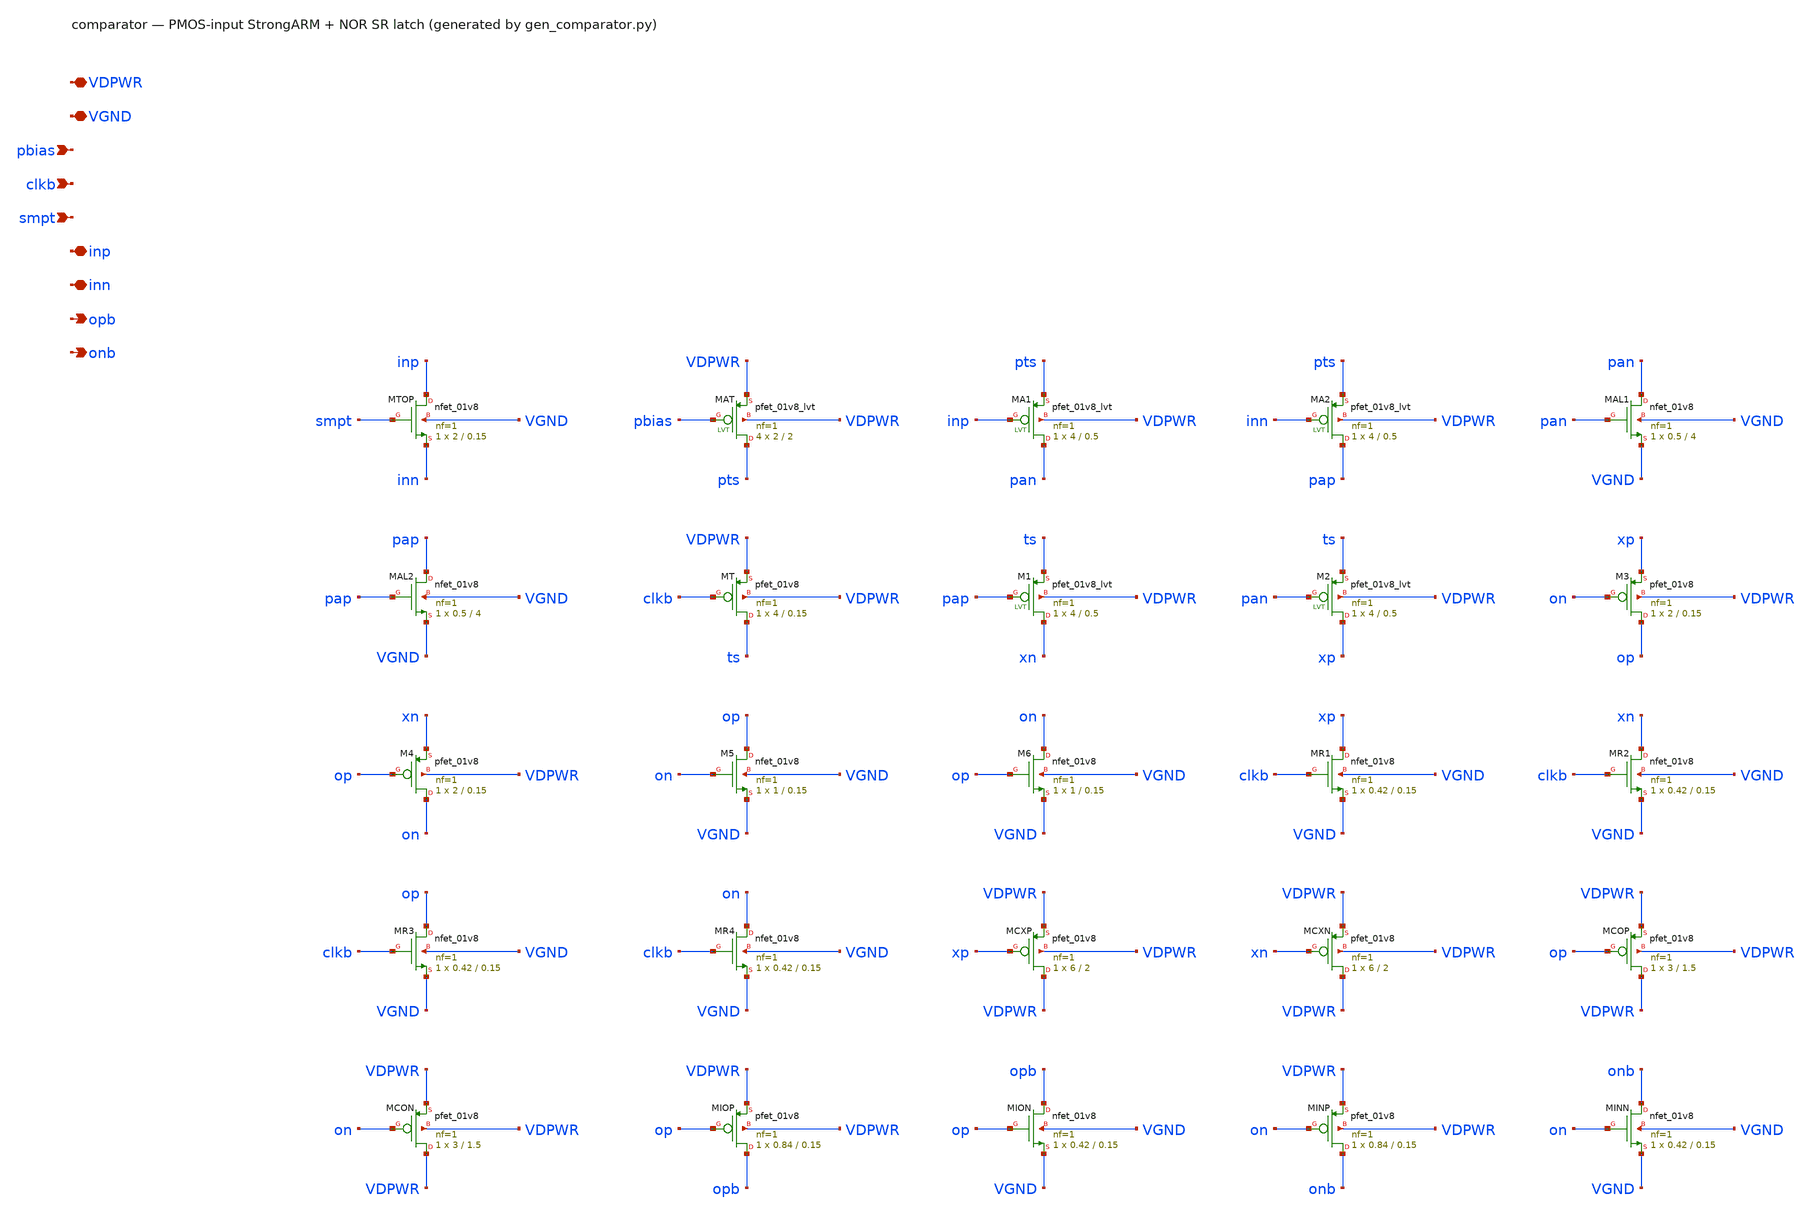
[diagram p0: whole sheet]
** sch_path: xschem/comparator.sch
**.subckt comparator VDPWR VGND pbias clkb smpt inp inn opb onb
*.iopin VDPWR
*.iopin VGND
*.ipin pbias
*.ipin clkb
*.ipin smpt
*.iopin inp
*.iopin inn
*.opin opb
*.opin onb
XMTOP inp smpt inn VGND sky130_fd_pr__nfet_01v8 L=0.15 W=2 nf=1 ad='int((1 + 1)/2) * 2 / 1 * 0.29' as='int((1 + 2)/2) * 2 / 1 * 0.29'
+ pd='2*int((1 + 1)/2) * (2 / 1 + 0.29)' ps='2*int((1 + 2)/2) * (2 / 1 + 0.29)' nrd='0.29 / 2 ' nrs='0.29 / 2 '
+ sa=0 sb=0 sd=0 mult=1 m=1
XMAT pts pbias VDPWR VDPWR sky130_fd_pr__pfet_01v8_lvt L=2 W=2 nf=1 ad='int((1 + 1)/2) * 2 / 1 * 0.29'
+ as='int((1 + 2)/2) * 2 / 1 * 0.29' pd='2*int((1 + 1)/2) * (2 / 1 + 0.29)' ps='2*int((1 + 2)/2) * (2 / 1 + 0.29)'
+ nrd='0.29 / 2 ' nrs='0.29 / 2 ' sa=0 sb=0 sd=0 mult=4 m=4
XMA1 pan inp pts VDPWR sky130_fd_pr__pfet_01v8_lvt L=0.5 W=4 nf=1 ad='int((1 + 1)/2) * 4 / 1 * 0.29'
+ as='int((1 + 2)/2) * 4 / 1 * 0.29' pd='2*int((1 + 1)/2) * (4 / 1 + 0.29)' ps='2*int((1 + 2)/2) * (4 / 1 + 0.29)'
+ nrd='0.29 / 4 ' nrs='0.29 / 4 ' sa=0 sb=0 sd=0 mult=1 m=1
XMA2 pap inn pts VDPWR sky130_fd_pr__pfet_01v8_lvt L=0.5 W=4 nf=1 ad='int((1 + 1)/2) * 4 / 1 * 0.29'
+ as='int((1 + 2)/2) * 4 / 1 * 0.29' pd='2*int((1 + 1)/2) * (4 / 1 + 0.29)' ps='2*int((1 + 2)/2) * (4 / 1 + 0.29)'
+ nrd='0.29 / 4 ' nrs='0.29 / 4 ' sa=0 sb=0 sd=0 mult=1 m=1
XMAL1 pan pan VGND VGND sky130_fd_pr__nfet_01v8 L=4 W=0.5 nf=1 ad='int((1 + 1)/2) * 0.5 / 1 * 0.29' as='int((1 + 2)/2) * 0.5 / 1 * 0.29'
+ pd='2*int((1 + 1)/2) * (0.5 / 1 + 0.29)' ps='2*int((1 + 2)/2) * (0.5 / 1 + 0.29)' nrd='0.29 / 0.5 ' nrs='0.29 / 0.5 '
+ sa=0 sb=0 sd=0 mult=1 m=1
XMAL2 pap pap VGND VGND sky130_fd_pr__nfet_01v8 L=4 W=0.5 nf=1 ad='int((1 + 1)/2) * 0.5 / 1 * 0.29' as='int((1 + 2)/2) * 0.5 / 1 * 0.29'
+ pd='2*int((1 + 1)/2) * (0.5 / 1 + 0.29)' ps='2*int((1 + 2)/2) * (0.5 / 1 + 0.29)' nrd='0.29 / 0.5 ' nrs='0.29 / 0.5 '
+ sa=0 sb=0 sd=0 mult=1 m=1
XMT ts clkb VDPWR VDPWR sky130_fd_pr__pfet_01v8 L=0.15 W=4 nf=1 ad='int((nf+1)/2) * W/nf * 0.29' as='int((nf+2)/2) * W/nf * 0.29'
+ pd='2*int((nf+1)/2) * (W/nf + 0.29)' ps='2*int((nf+2)/2) * (W/nf + 0.29)' nrd='0.29 / W' nrs='0.29 / W'
+ sa=0 sb=0 sd=0 mult=1 m=1
XM1 xn pap ts VDPWR sky130_fd_pr__pfet_01v8_lvt L=0.5 W=4 nf=1 ad='int((1 + 1)/2) * 4 / 1 * 0.29' as='int((1 + 2)/2) * 4 / 1 * 0.29'
+ pd='2*int((1 + 1)/2) * (4 / 1 + 0.29)' ps='2*int((1 + 2)/2) * (4 / 1 + 0.29)' nrd='0.29 / 4 ' nrs='0.29 / 4 '
+ sa=0 sb=0 sd=0 mult=1 m=1
XM2 xp pan ts VDPWR sky130_fd_pr__pfet_01v8_lvt L=0.5 W=4 nf=1 ad='int((1 + 1)/2) * 4 / 1 * 0.29' as='int((1 + 2)/2) * 4 / 1 * 0.29'
+ pd='2*int((1 + 1)/2) * (4 / 1 + 0.29)' ps='2*int((1 + 2)/2) * (4 / 1 + 0.29)' nrd='0.29 / 4 ' nrs='0.29 / 4 '
+ sa=0 sb=0 sd=0 mult=1 m=1
XM3 op on xp VDPWR sky130_fd_pr__pfet_01v8 L=0.15 W=2 nf=1 ad='int((nf+1)/2) * W/nf * 0.29' as='int((nf+2)/2) * W/nf * 0.29'
+ pd='2*int((nf+1)/2) * (W/nf + 0.29)' ps='2*int((nf+2)/2) * (W/nf + 0.29)' nrd='0.29 / W' nrs='0.29 / W'
+ sa=0 sb=0 sd=0 mult=1 m=1
XM4 on op xn VDPWR sky130_fd_pr__pfet_01v8 L=0.15 W=2 nf=1 ad='int((nf+1)/2) * W/nf * 0.29' as='int((nf+2)/2) * W/nf * 0.29'
+ pd='2*int((nf+1)/2) * (W/nf + 0.29)' ps='2*int((nf+2)/2) * (W/nf + 0.29)' nrd='0.29 / W' nrs='0.29 / W'
+ sa=0 sb=0 sd=0 mult=1 m=1
XM5 op on VGND VGND sky130_fd_pr__nfet_01v8 L=0.15 W=1 nf=1 ad='int((1 + 1)/2) * 1 / 1 * 0.29' as='int((1 + 2)/2) * 1 / 1 * 0.29'
+ pd='2*int((1 + 1)/2) * (1 / 1 + 0.29)' ps='2*int((1 + 2)/2) * (1 / 1 + 0.29)' nrd='0.29 / 1 ' nrs='0.29 / 1 '
+ sa=0 sb=0 sd=0 mult=1 m=1
XM6 on op VGND VGND sky130_fd_pr__nfet_01v8 L=0.15 W=1 nf=1 ad='int((1 + 1)/2) * 1 / 1 * 0.29' as='int((1 + 2)/2) * 1 / 1 * 0.29'
+ pd='2*int((1 + 1)/2) * (1 / 1 + 0.29)' ps='2*int((1 + 2)/2) * (1 / 1 + 0.29)' nrd='0.29 / 1 ' nrs='0.29 / 1 '
+ sa=0 sb=0 sd=0 mult=1 m=1
XMR1 xp clkb VGND VGND sky130_fd_pr__nfet_01v8 L=0.15 W=0.42 nf=1 ad='int((1 + 1)/2) * 0.42 / 1 * 0.29'
+ as='int((1 + 2)/2) * 0.42 / 1 * 0.29' pd='2*int((1 + 1)/2) * (0.42 / 1 + 0.29)' ps='2*int((1 + 2)/2) * (0.42 / 1 + 0.29)'
+ nrd='0.29 / 0.42 ' nrs='0.29 / 0.42 ' sa=0 sb=0 sd=0 mult=1 m=1
XMR2 xn clkb VGND VGND sky130_fd_pr__nfet_01v8 L=0.15 W=0.42 nf=1 ad='int((1 + 1)/2) * 0.42 / 1 * 0.29'
+ as='int((1 + 2)/2) * 0.42 / 1 * 0.29' pd='2*int((1 + 1)/2) * (0.42 / 1 + 0.29)' ps='2*int((1 + 2)/2) * (0.42 / 1 + 0.29)'
+ nrd='0.29 / 0.42 ' nrs='0.29 / 0.42 ' sa=0 sb=0 sd=0 mult=1 m=1
XMR3 op clkb VGND VGND sky130_fd_pr__nfet_01v8 L=0.15 W=0.42 nf=1 ad='int((1 + 1)/2) * 0.42 / 1 * 0.29'
+ as='int((1 + 2)/2) * 0.42 / 1 * 0.29' pd='2*int((1 + 1)/2) * (0.42 / 1 + 0.29)' ps='2*int((1 + 2)/2) * (0.42 / 1 + 0.29)'
+ nrd='0.29 / 0.42 ' nrs='0.29 / 0.42 ' sa=0 sb=0 sd=0 mult=1 m=1
XMR4 on clkb VGND VGND sky130_fd_pr__nfet_01v8 L=0.15 W=0.42 nf=1 ad='int((1 + 1)/2) * 0.42 / 1 * 0.29'
+ as='int((1 + 2)/2) * 0.42 / 1 * 0.29' pd='2*int((1 + 1)/2) * (0.42 / 1 + 0.29)' ps='2*int((1 + 2)/2) * (0.42 / 1 + 0.29)'
+ nrd='0.29 / 0.42 ' nrs='0.29 / 0.42 ' sa=0 sb=0 sd=0 mult=1 m=1
XMCXP VDPWR xp VDPWR VDPWR sky130_fd_pr__pfet_01v8 L=2 W=6 nf=1 ad='int((nf+1)/2) * W/nf * 0.29' as='int((nf+2)/2) * W/nf * 0.29'
+ pd='2*int((nf+1)/2) * (W/nf + 0.29)' ps='2*int((nf+2)/2) * (W/nf + 0.29)' nrd='0.29 / W' nrs='0.29 / W'
+ sa=0 sb=0 sd=0 mult=1 m=1
XMCXN VDPWR xn VDPWR VDPWR sky130_fd_pr__pfet_01v8 L=2 W=6 nf=1 ad='int((nf+1)/2) * W/nf * 0.29' as='int((nf+2)/2) * W/nf * 0.29'
+ pd='2*int((nf+1)/2) * (W/nf + 0.29)' ps='2*int((nf+2)/2) * (W/nf + 0.29)' nrd='0.29 / W' nrs='0.29 / W'
+ sa=0 sb=0 sd=0 mult=1 m=1
XMCOP VDPWR op VDPWR VDPWR sky130_fd_pr__pfet_01v8 L=1.5 W=3 nf=1 ad='int((nf+1)/2) * W/nf * 0.29' as='int((nf+2)/2) * W/nf * 0.29'
+ pd='2*int((nf+1)/2) * (W/nf + 0.29)' ps='2*int((nf+2)/2) * (W/nf + 0.29)' nrd='0.29 / W' nrs='0.29 / W'
+ sa=0 sb=0 sd=0 mult=1 m=1
XMCON VDPWR on VDPWR VDPWR sky130_fd_pr__pfet_01v8 L=1.5 W=3 nf=1 ad='int((nf+1)/2) * W/nf * 0.29' as='int((nf+2)/2) * W/nf * 0.29'
+ pd='2*int((nf+1)/2) * (W/nf + 0.29)' ps='2*int((nf+2)/2) * (W/nf + 0.29)' nrd='0.29 / W' nrs='0.29 / W'
+ sa=0 sb=0 sd=0 mult=1 m=1
XMIOP opb op VDPWR VDPWR sky130_fd_pr__pfet_01v8 L=0.15 W=0.84 nf=1 ad='int((nf+1)/2) * W/nf * 0.29'
+ as='int((nf+2)/2) * W/nf * 0.29' pd='2*int((nf+1)/2) * (W/nf + 0.29)' ps='2*int((nf+2)/2) * (W/nf + 0.29)'
+ nrd='0.29 / W' nrs='0.29 / W' sa=0 sb=0 sd=0 mult=1 m=1
XMION opb op VGND VGND sky130_fd_pr__nfet_01v8 L=0.15 W=0.42 nf=1 ad='int((1 + 1)/2) * 0.42 / 1 * 0.29'
+ as='int((1 + 2)/2) * 0.42 / 1 * 0.29' pd='2*int((1 + 1)/2) * (0.42 / 1 + 0.29)' ps='2*int((1 + 2)/2) * (0.42 / 1 + 0.29)'
+ nrd='0.29 / 0.42 ' nrs='0.29 / 0.42 ' sa=0 sb=0 sd=0 mult=1 m=1
XMINP onb on VDPWR VDPWR sky130_fd_pr__pfet_01v8 L=0.15 W=0.84 nf=1 ad='int((nf+1)/2) * W/nf * 0.29'
+ as='int((nf+2)/2) * W/nf * 0.29' pd='2*int((nf+1)/2) * (W/nf + 0.29)' ps='2*int((nf+2)/2) * (W/nf + 0.29)'
+ nrd='0.29 / W' nrs='0.29 / W' sa=0 sb=0 sd=0 mult=1 m=1
XMINN onb on VGND VGND sky130_fd_pr__nfet_01v8 L=0.15 W=0.42 nf=1 ad='int((1 + 1)/2) * 0.42 / 1 * 0.29'
+ as='int((1 + 2)/2) * 0.42 / 1 * 0.29' pd='2*int((1 + 1)/2) * (0.42 / 1 + 0.29)' ps='2*int((1 + 2)/2) * (0.42 / 1 + 0.29)'
+ nrd='0.29 / 0.42 ' nrs='0.29 / 0.42 ' sa=0 sb=0 sd=0 mult=1 m=1
**.ends
.end
